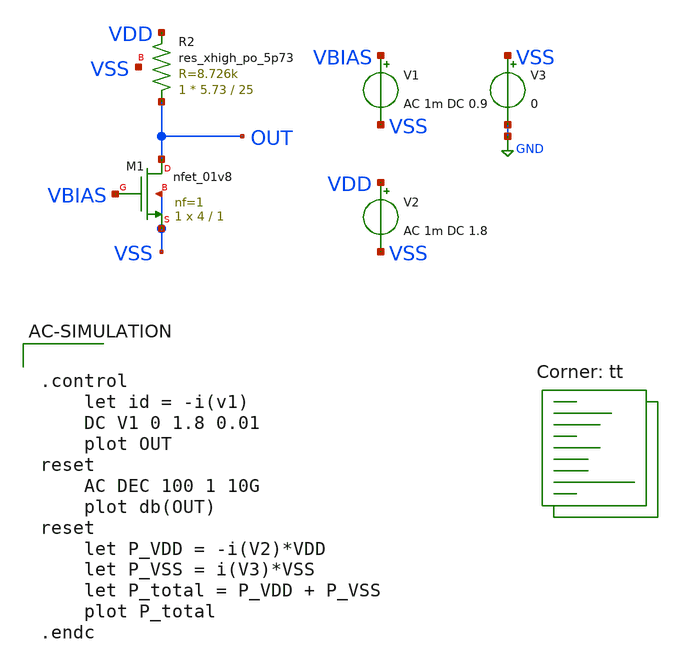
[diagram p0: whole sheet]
** sch_path: designs/libs/core_analog/p-ota/cs-amp.sch
**.subckt cs-amp
XM1 OUT VBIAS VSS VSS sky130_fd_pr__nfet_01v8 L=1 W=4 nf=1 ad='int((nf+1)/2) * W/nf * 0.29' as='int((nf+2)/2) * W/nf * 0.29'
+ pd='2*int((nf+1)/2) * (W/nf + 0.29)' ps='2*int((nf+2)/2) * (W/nf + 0.29)' nrd='0.29 / W' nrs='0.29 / W'
+ sa=0 sb=0 sd=0 mult=1 m=1
V1 VBIAS VSS AC 1m DC 0.9
V2 VDD VSS AC 1m DC 1.8
V3 VSS GND 0
XR2 OUT VDD VSS sky130_fd_pr__res_xhigh_po_5p73 L=25 mult=1 m=1
**** begin user architecture code
.lib $::SKYWATER_MODELS/sky130.lib.spice tt


.control
	let id = -i(v1)
	DC V1 0 1.8 0.01
	plot OUT
reset
	AC DEC 100 1 10G
	plot db(OUT)
reset
	let P_VDD = -i(V2)*VDD
	let P_VSS = i(V3)*VSS
	let P_total = P_VDD + P_VSS
	plot P_total
.endc

**** end user architecture code
**.ends
.GLOBAL GND
.end
